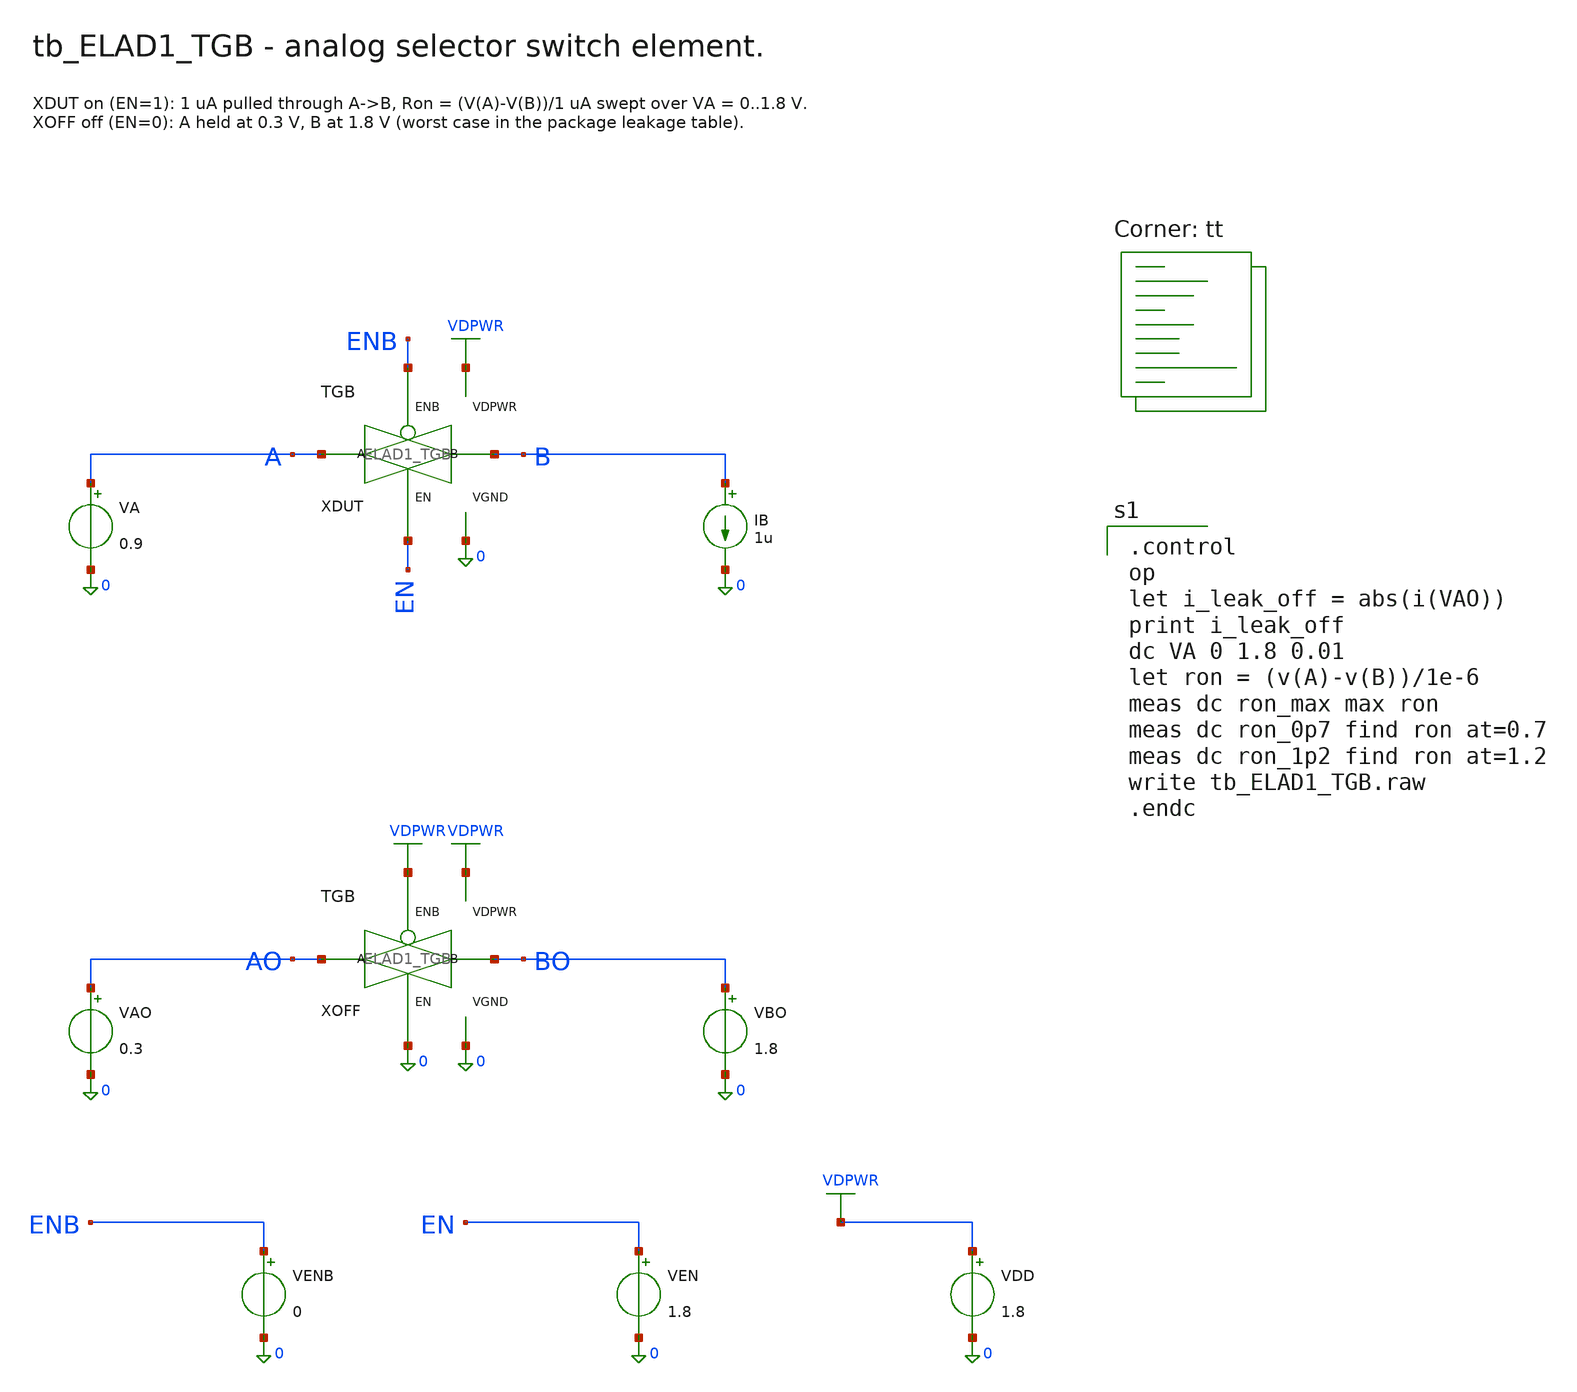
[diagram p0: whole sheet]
** sch_path: cells/ELAD1_TGB/schematic/tb_ELAD1_TGB.sch
**.subckt tb_ELAD1_TGB
XDUT A B EN ENB VDPWR 0 ELAD1_TGB
VA A 0 0.9
IB B 0 1u
XOFF AO BO 0 VDPWR VDPWR 0 ELAD1_TGB
VAO AO 0 0.3
VBO BO 0 1.8
VENB ENB 0 0
VEN EN 0 1.8
VDD VDPWR 0 1.8
**** begin user architecture code

.control
op
let i_leak_off = abs(i(VAO))
print i_leak_off
dc VA 0 1.8 0.01
let ron = (v(A)-v(B))/1e-6
meas dc ron_max max ron
meas dc ron_0p7 find ron at=0.7
meas dc ron_1p2 find ron at=1.2
write tb_ELAD1_TGB.raw
.endc

.lib $::SKYWATER_MODELS/sky130.lib.spice tt
**** end user architecture code
**.ends

* expanding   symbol:  ELAD1_TGB.sym # of pins=6
** sym_path: cells/ELAD1_TGB/schematic/ELAD1_TGB.sym
** sch_path: cells/ELAD1_TGB/schematic/ELAD1_TGB.sch
.subckt ELAD1_TGB A B EN ENB VDPWR VGND
*.iopin A
*.iopin B
*.iopin EN
*.iopin ENB
*.iopin VDPWR
*.iopin VGND
XMN A EN B VGND sky130_fd_pr__nfet_01v8 L=0.15 W=1 nf=1 ad='int((1 + 1)/2) * 1 / 1 * 0.29' as='int((1 + 2)/2) * 1 / 1 * 0.29'
+ pd='2*int((1 + 1)/2) * (1 / 1 + 0.29)' ps='2*int((1 + 2)/2) * (1 / 1 + 0.29)' nrd='0.29 / 1 ' nrs='0.29 / 1 '
+ sa=0 sb=0 sd=0 mult=1 m=1
XMP A ENB B VDPWR sky130_fd_pr__pfet_01v8 L=0.15 W=2 nf=1 ad='int((nf+1)/2) * W/nf * 0.29' as='int((nf+2)/2) * W/nf * 0.29'
+ pd='2*int((nf+1)/2) * (W/nf + 0.29)' ps='2*int((nf+2)/2) * (W/nf + 0.29)' nrd='0.29 / W' nrs='0.29 / W'
+ sa=0 sb=0 sd=0 mult=1 m=1
.ends

.end
